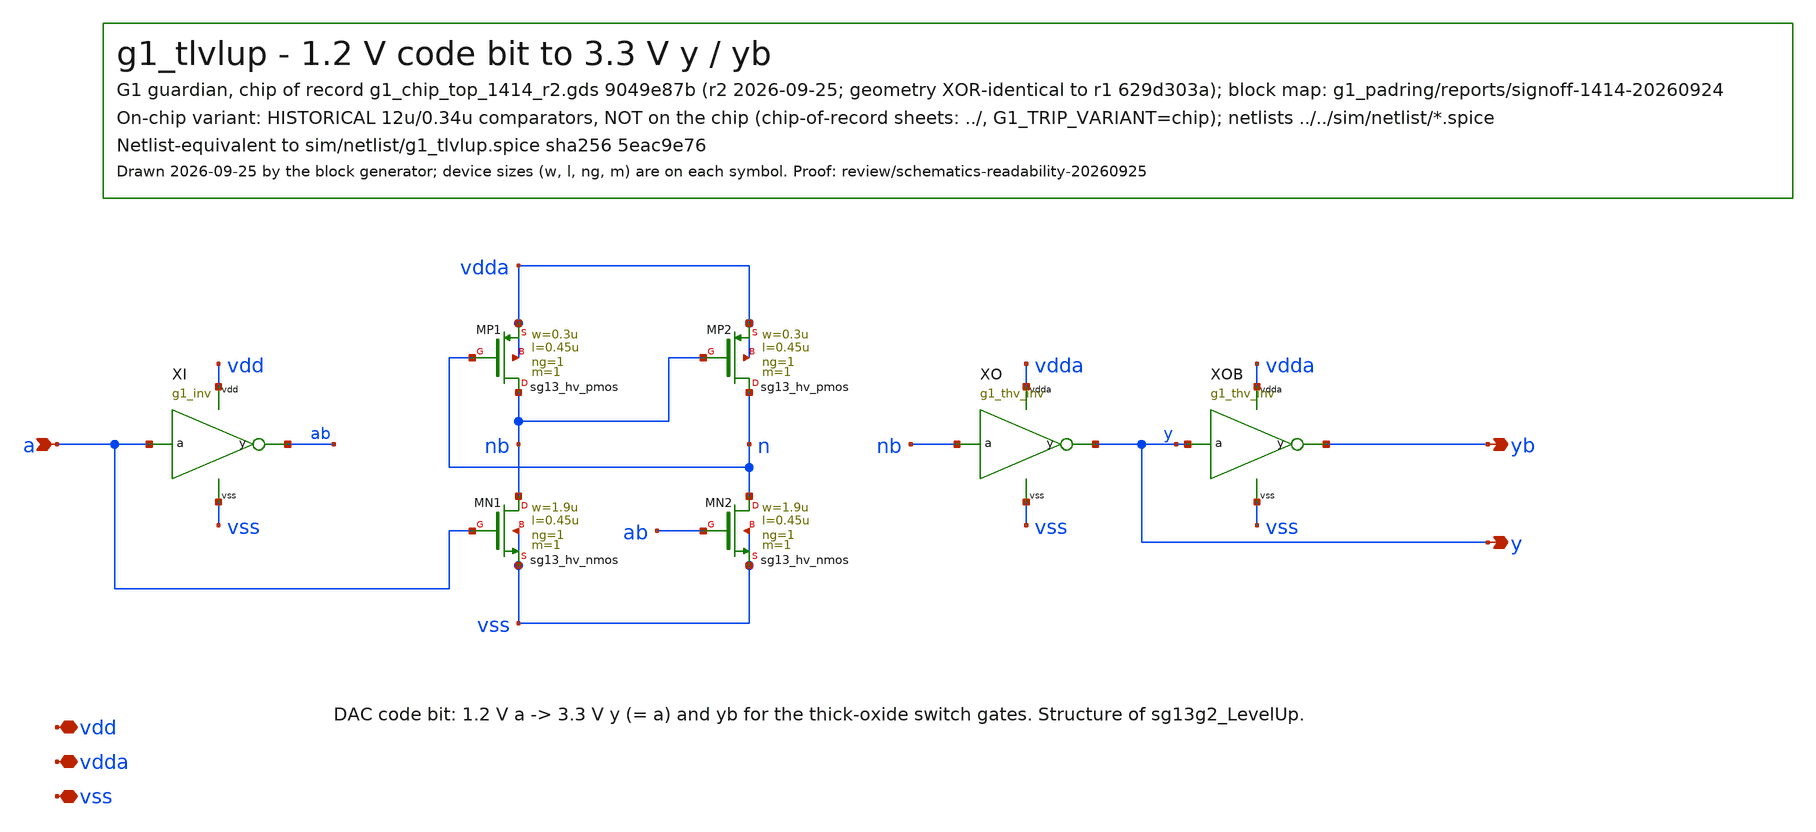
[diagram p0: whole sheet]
** sch_path: designs/g1-guardian/blocks/g1_trip/schematic/historical_12u034/g1_tlvlup.sch
**.subckt g1_tlvlup a y yb vdd vdda vss
*.ipin a
*.opin y
*.opin yb
*.iopin vdd
*.iopin vdda
*.iopin vss
XI a ab vdd vss g1_inv
XMN1 nb a vss vss sg13_hv_nmos w=1.9u l=0.45u ng=1 m=1 mm_ok=1
XMN2 n ab vss vss sg13_hv_nmos w=1.9u l=0.45u ng=1 m=1 mm_ok=1
XMP1 nb n vdda vdda sg13_hv_pmos w=0.3u l=0.45u ng=1 m=1 mm_ok=1
XMP2 n nb vdda vdda sg13_hv_pmos w=0.3u l=0.45u ng=1 m=1 mm_ok=1
XO nb y vdda vss g1_thv_inv
XOB y yb vdda vss g1_thv_inv
**.ends

* expanding   symbol:  g1_inv.sym # of pins=4
** sym_path: designs/g1-guardian/blocks/g1_trip/schematic/historical_12u034/g1_inv.sym
** sch_path: designs/g1-guardian/blocks/g1_trip/schematic/historical_12u034/g1_inv.sch
.subckt g1_inv a y vdd vss
*.ipin a
*.opin y
*.iopin vdd
*.iopin vss
XMP y a vdd vdd sg13_lv_pmos w=1u l=0.13u ng=1 m=1 mm_ok=1
XMN y a vss vss sg13_lv_nmos w=0.5u l=0.13u ng=1 m=1 mm_ok=1
.ends


* expanding   symbol:  g1_thv_inv.sym # of pins=4
** sym_path: designs/g1-guardian/blocks/g1_trip/schematic/historical_12u034/g1_thv_inv.sym
** sch_path: designs/g1-guardian/blocks/g1_trip/schematic/historical_12u034/g1_thv_inv.sch
.subckt g1_thv_inv a y vdda vss
*.ipin a
*.opin y
*.iopin vdda
*.iopin vss
XMP y a vdda vdda sg13_hv_pmos w=3.9u l=0.45u ng=1 m=1 mm_ok=1
XMN y a vss vss sg13_hv_nmos w=1.9u l=0.45u ng=1 m=1 mm_ok=1
.ends

.end
